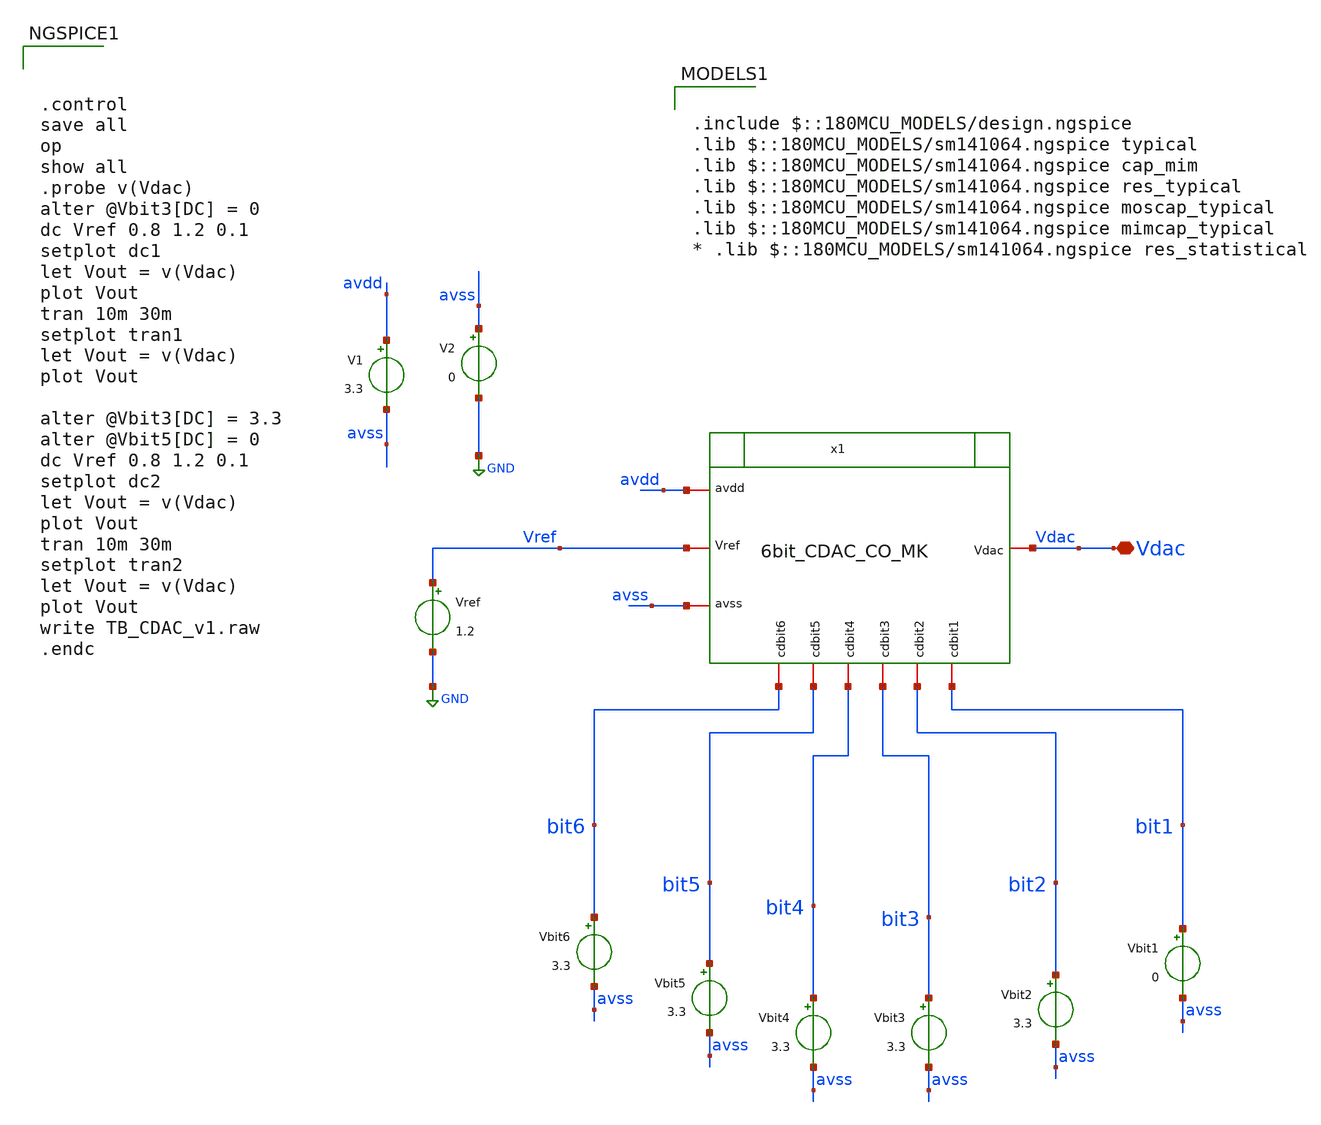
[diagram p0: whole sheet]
** sch_path: designs/libs/WK_Kadam/TB_6bit_CDAC_CO_V1_MK.sch
**.subckt TB_6bit_CDAC_CO_V1_MK Vdac
*.iopin Vdac
x1 Vdac avdd avss Vref bit6 bit5 bit3 bit1 bit2 bit4 6bit_CDAC_CO_MK
V1 avdd avss 3.3
V2 avss GND 0
Vbit1 bit1 avss 0
Vbit2 bit2 avss 3.3
Vbit3 bit3 avss 3.3
Vbit4 bit4 avss 3.3
Vbit5 bit5 avss 3.3
Vbit6 bit6 avss 3.3
Vref Vref GND 1.2
**** begin user architecture code



.control
save all
op
show all
.probe v(Vdac)
alter @Vbit3[DC] = 0
dc Vref 0.8 1.2 0.1
setplot dc1
let Vout = v(Vdac)
plot Vout
tran 10m 30m
setplot tran1
let Vout = v(Vdac)
plot Vout

alter @Vbit3[DC] = 3.3
alter @Vbit5[DC] = 0
dc Vref 0.8 1.2 0.1
setplot dc2
let Vout = v(Vdac)
plot Vout
tran 10m 30m
setplot tran2
let Vout = v(Vdac)
plot Vout
write TB_CDAC_v1.raw
.endc



.include $::180MCU_MODELS/design.ngspice
.lib $::180MCU_MODELS/sm141064.ngspice typical
.lib $::180MCU_MODELS/sm141064.ngspice cap_mim
.lib $::180MCU_MODELS/sm141064.ngspice res_typical
.lib $::180MCU_MODELS/sm141064.ngspice moscap_typical
.lib $::180MCU_MODELS/sm141064.ngspice mimcap_typical
* .lib $::180MCU_MODELS/sm141064.ngspice res_statistical

**** end user architecture code
**.ends
.GLOBAL GND
.end
